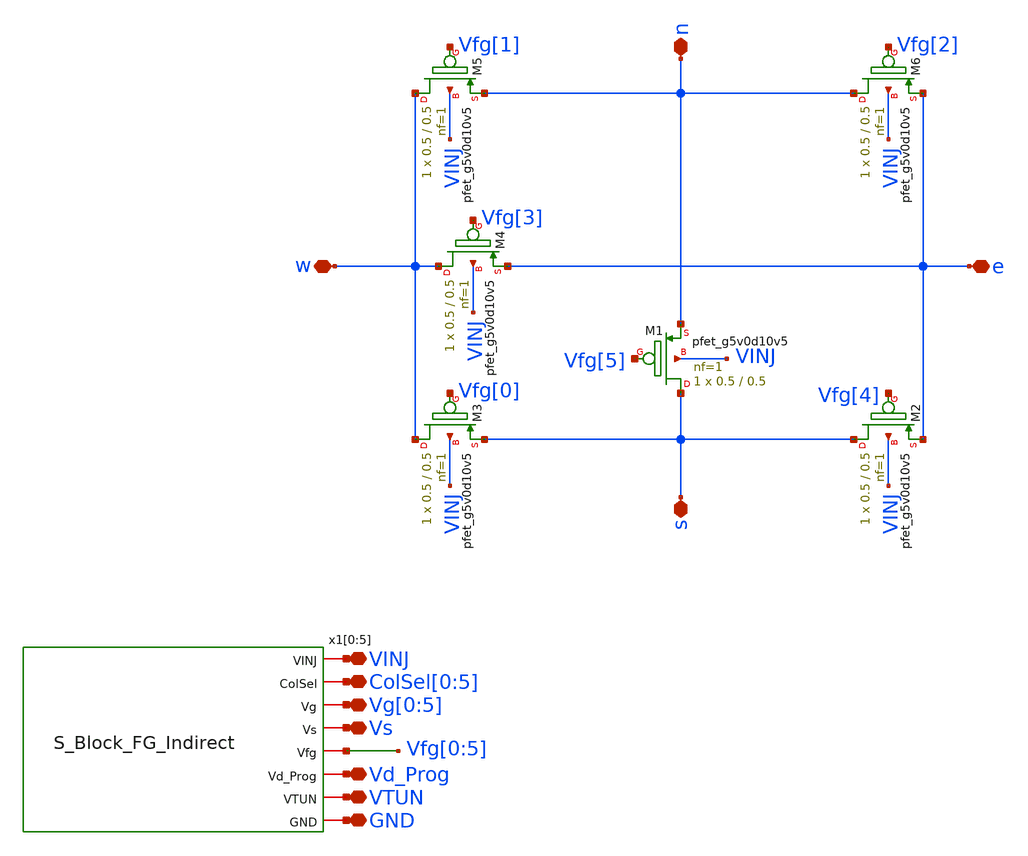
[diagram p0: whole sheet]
** sch_path: sky130_cells/Sblock/S_Block.sch
**.subckt S_Block s w n e VINJ ColSel[0],ColSel[1],ColSel[2],ColSel[3],ColSel[4],ColSel[5]
*+ Vg[0],Vg[1],Vg[2],Vg[3],Vg[4],Vg[5] Vs Vd_Prog VTUN GND
*.iopin s
*.iopin w
*.iopin n
*.iopin e
*.iopin VINJ
*.iopin ColSel[0],ColSel[1],ColSel[2],ColSel[3],ColSel[4],ColSel[5]
*.iopin Vg[0],Vg[1],Vg[2],Vg[3],Vg[4],Vg[5]
*.iopin Vs
*.iopin Vd_Prog
*.iopin VTUN
*.iopin GND
XM1 s Vfg[5] n VINJ sky130_fd_pr__pfet_g5v0d10v5 L=0.5 W=0.5 nf=1 ad='int((1 + 1)/2) * 0.5 / 1 * 0.29'
+ as='int((1 + 2)/2) * 0.5 / 1 * 0.29' pd='2*int((1 + 1)/2) * (0.5 / 1 + 0.29)' ps='2*int((1 + 2)/2) * (0.5 / 1 + 0.29)'
+ nrd='0.29 / 0.5 ' nrs='0.29 / 0.5 ' sa=0 sb=0 sd=0 mult=1 m=1
XM2 s Vfg[4] e VINJ sky130_fd_pr__pfet_g5v0d10v5 L=0.5 W=0.5 nf=1 ad='int((1 + 1)/2) * 0.5 / 1 * 0.29'
+ as='int((1 + 2)/2) * 0.5 / 1 * 0.29' pd='2*int((1 + 1)/2) * (0.5 / 1 + 0.29)' ps='2*int((1 + 2)/2) * (0.5 / 1 + 0.29)'
+ nrd='0.29 / 0.5 ' nrs='0.29 / 0.5 ' sa=0 sb=0 sd=0 mult=1 m=1
XM3 w Vfg[0] s VINJ sky130_fd_pr__pfet_g5v0d10v5 L=0.5 W=0.5 nf=1 ad='int((1 + 1)/2) * 0.5 / 1 * 0.29'
+ as='int((1 + 2)/2) * 0.5 / 1 * 0.29' pd='2*int((1 + 1)/2) * (0.5 / 1 + 0.29)' ps='2*int((1 + 2)/2) * (0.5 / 1 + 0.29)'
+ nrd='0.29 / 0.5 ' nrs='0.29 / 0.5 ' sa=0 sb=0 sd=0 mult=1 m=1
XM4 w Vfg[3] e VINJ sky130_fd_pr__pfet_g5v0d10v5 L=0.5 W=0.5 nf=1 ad='int((1 + 1)/2) * 0.5 / 1 * 0.29'
+ as='int((1 + 2)/2) * 0.5 / 1 * 0.29' pd='2*int((1 + 1)/2) * (0.5 / 1 + 0.29)' ps='2*int((1 + 2)/2) * (0.5 / 1 + 0.29)'
+ nrd='0.29 / 0.5 ' nrs='0.29 / 0.5 ' sa=0 sb=0 sd=0 mult=1 m=1
XM5 w Vfg[1] n VINJ sky130_fd_pr__pfet_g5v0d10v5 L=0.5 W=0.5 nf=1 ad='int((1 + 1)/2) * 0.5 / 1 * 0.29'
+ as='int((1 + 2)/2) * 0.5 / 1 * 0.29' pd='2*int((1 + 1)/2) * (0.5 / 1 + 0.29)' ps='2*int((1 + 2)/2) * (0.5 / 1 + 0.29)'
+ nrd='0.29 / 0.5 ' nrs='0.29 / 0.5 ' sa=0 sb=0 sd=0 mult=1 m=1
XM6 n Vfg[2] e VINJ sky130_fd_pr__pfet_g5v0d10v5 L=0.5 W=0.5 nf=1 ad='int((1 + 1)/2) * 0.5 / 1 * 0.29'
+ as='int((1 + 2)/2) * 0.5 / 1 * 0.29' pd='2*int((1 + 1)/2) * (0.5 / 1 + 0.29)' ps='2*int((1 + 2)/2) * (0.5 / 1 + 0.29)'
+ nrd='0.29 / 0.5 ' nrs='0.29 / 0.5 ' sa=0 sb=0 sd=0 mult=1 m=1
x1[0] VINJ ColSel[0] Vg[0] Vs net1[5] Vd_Prog VTUN GND S_Block_FG_Indirect
x1[1] VINJ ColSel[1] Vg[1] Vs net1[4] Vd_Prog VTUN GND S_Block_FG_Indirect
x1[2] VINJ ColSel[2] Vg[2] Vs net1[3] Vd_Prog VTUN GND S_Block_FG_Indirect
x1[3] VINJ ColSel[3] Vg[3] Vs net1[2] Vd_Prog VTUN GND S_Block_FG_Indirect
x1[4] VINJ ColSel[4] Vg[4] Vs net1[1] Vd_Prog VTUN GND S_Block_FG_Indirect
x1[5] VINJ ColSel[5] Vg[5] Vs net1[0] Vd_Prog VTUN GND S_Block_FG_Indirect
**.ends

* expanding   symbol:  sky130_cells/Sblock/S_Block_FG_Indirect.sym # of pins=8
** sym_path: sky130_cells/Sblock/S_Block_FG_Indirect.sym
** sch_path: sky130_cells/Sblock/S_Block_FG_Indirect.sch
.subckt S_Block_FG_Indirect VINJ ColSel Vg Vs Vfg Vd_Prog VTUN GND
*.iopin VINJ
*.iopin ColSel
*.iopin Vg
*.iopin Vs
*.iopin Vfg
*.iopin Vd_Prog
*.iopin VTUN
*.iopin GND
XM2 net1 ColSel VINJ VINJ sky130_fd_pr__pfet_g5v0d10v5 L=0.5 W=0.42 nf=1 ad='int((nf+1)/2) * W/nf * 0.29'
+ as='int((nf+2)/2) * W/nf * 0.29' pd='2*int((nf+1)/2) * (W/nf + 0.29)' ps='2*int((nf+2)/2) * (W/nf + 0.29)'
+ nrd='0.29 / W' nrs='0.29 / W' sa=0 sb=0 sd=0 mult=1 m=1
XM3 Vd_Prog Vfg net1 VINJ sky130_fd_pr__pfet_g5v0d10v5 L=0.5 W=0.42 nf=1 ad='int((nf+1)/2) * W/nf * 0.29'
+ as='int((nf+2)/2) * W/nf * 0.29' pd='2*int((nf+1)/2) * (W/nf + 0.29)' ps='2*int((nf+2)/2) * (W/nf + 0.29)'
+ nrd='0.29 / W' nrs='0.29 / W' sa=0 sb=0 sd=0 mult=1 m=1
XC1 Vfg VTUN GND sky130_fd_pr__cap_var_hvt W=0.29 L=0.5 VM=1 m=1
XC2 Vfg Vg GND sky130_fd_pr__cap_var_hvt W=0.54 L=0.65 VM=1 m=1
.ends

.end
